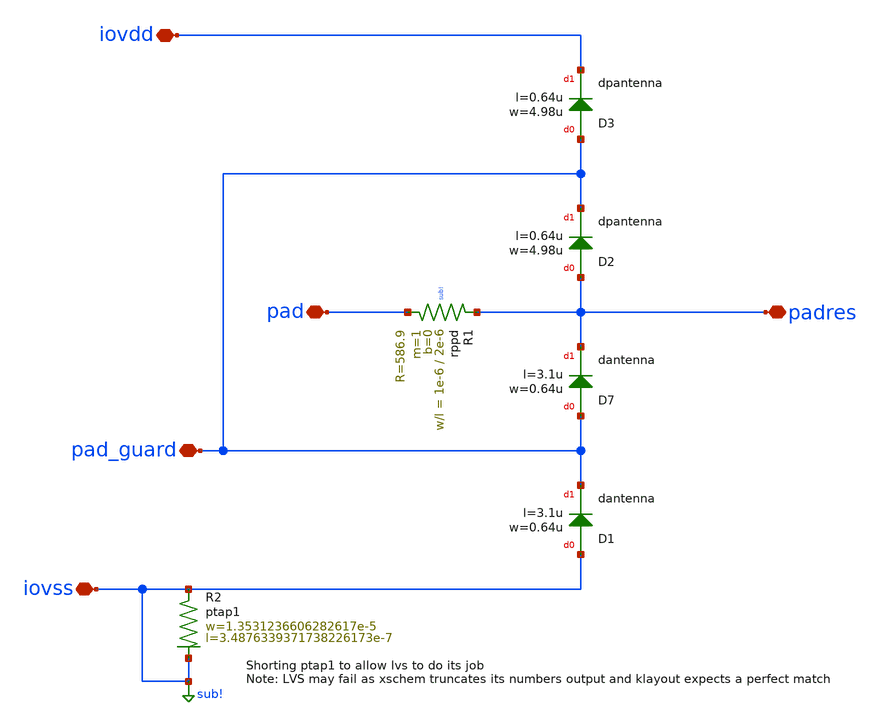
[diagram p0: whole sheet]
** sch_path: trident_test_structures/design_data/xschem/IOPadAnalogGuardLayer/secondary_protection_guard_layer.sch
**.subckt secondary_protection_guard_layer iovss iovdd pad pad_guard padres
*.iopin iovss
*.iopin iovdd
*.iopin pad
*.iopin pad_guard
*.iopin padres
XR1 padres pad sub! rppd w=1e-6 l=2e-6 m=1 b=0 mm_ok=1
XD7 pad_guard padres dantenna l=3.1u w=0.64u
XD1 iovss pad_guard dantenna l=3.1u w=0.64u
XD2 padres pad_guard dpantenna l=0.64u w=4.98u
XD3 pad_guard iovdd dpantenna l=0.64u w=4.98u
XR2 iovss iovss ptap1 R=30.17 w=1.3531236606282617e-5 l=3.4876339371738226173e-7
**.ends
.GLOBAL sub!
.end
